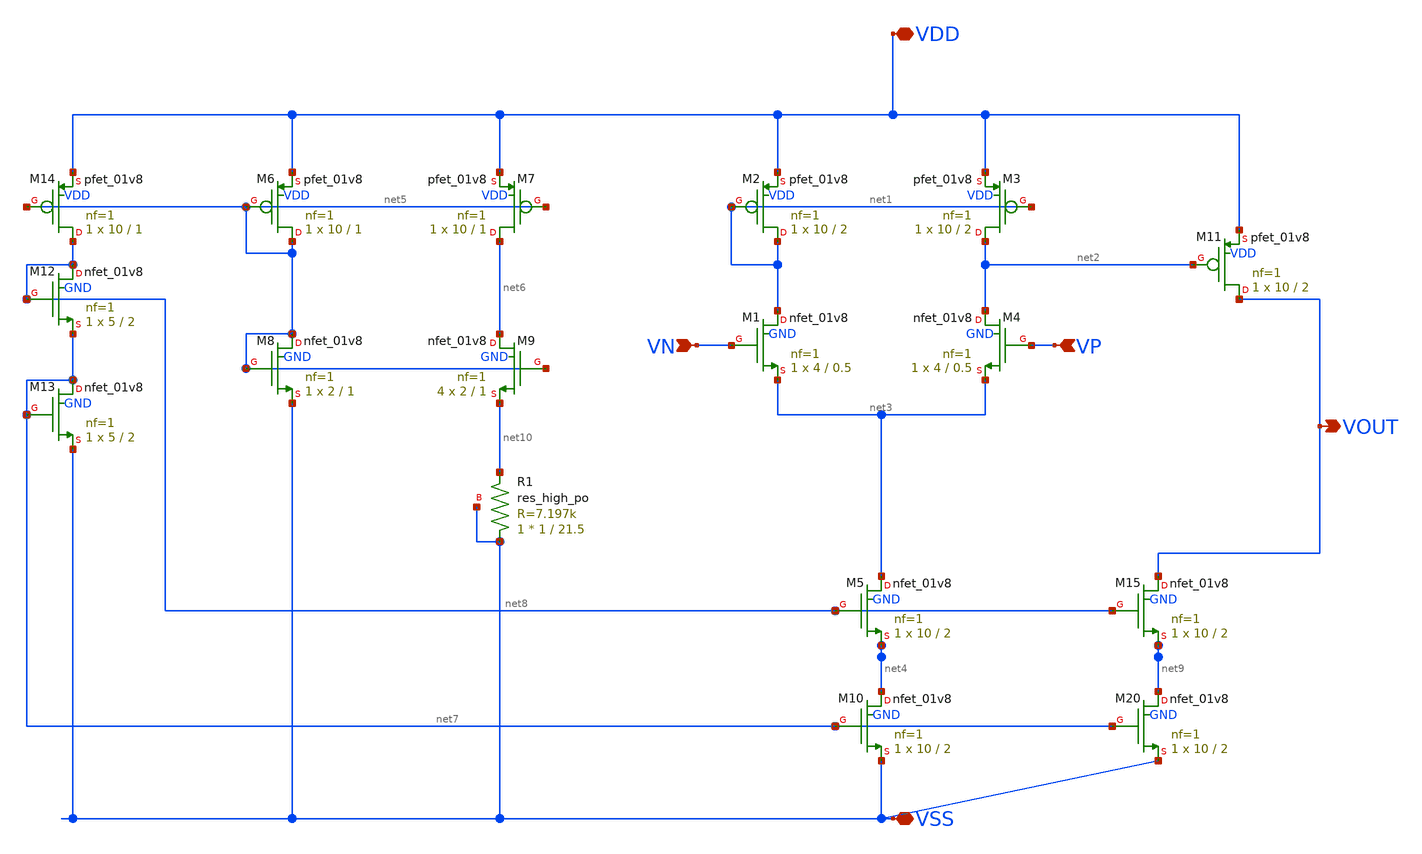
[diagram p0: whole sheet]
** sch_path: comparator.sch
**.subckt comparator VN VP VDD VOUT VSS
*.ipin VN
*.ipin VP
*.iopin VDD
*.opin VOUT
*.iopin VSS
XM2 net1 net1 VDD VDD sky130_fd_pr__pfet_01v8 L=2 W=10 nf=1 ad='int((1 + 1)/2) * 10 / 1 * 0.29' as='int((1 + 2)/2) * 10 / 1 * 0.29'
+ pd='2*int((1 + 1)/2) * (10 / 1 + 0.29)' ps='2*int((1 + 2)/2) * (10 / 1 + 0.29)' nrd='0.29 / 10 ' nrs='0.29 / 10 '
+ sa=0 sb=0 sd=0 mult=1 m=1
XM3 net2 net1 VDD VDD sky130_fd_pr__pfet_01v8 L=2 W=10 nf=1 ad='int((1 + 1)/2) * 10 / 1 * 0.29' as='int((1 + 2)/2) * 10 / 1 * 0.29'
+ pd='2*int((1 + 1)/2) * (10 / 1 + 0.29)' ps='2*int((1 + 2)/2) * (10 / 1 + 0.29)' nrd='0.29 / 10 ' nrs='0.29 / 10 '
+ sa=0 sb=0 sd=0 mult=1 m=1
XM1 net1 VN net3 GND sky130_fd_pr__nfet_01v8 L=0.5 W=4 nf=1 ad='int((1 + 1)/2) * 4 / 1 * 0.29' as='int((1 + 2)/2) * 4 / 1 * 0.29'
+ pd='2*int((1 + 1)/2) * (4 / 1 + 0.29)' ps='2*int((1 + 2)/2) * (4 / 1 + 0.29)' nrd='0.29 / 4 ' nrs='0.29 / 4 '
+ sa=0 sb=0 sd=0 mult=1 m=1
XM4 net2 VP net3 GND sky130_fd_pr__nfet_01v8 L=0.5 W=4 nf=1 ad='int((1 + 1)/2) * 4 / 1 * 0.29' as='int((1 + 2)/2) * 4 / 1 * 0.29'
+ pd='2*int((1 + 1)/2) * (4 / 1 + 0.29)' ps='2*int((1 + 2)/2) * (4 / 1 + 0.29)' nrd='0.29 / 4 ' nrs='0.29 / 4 '
+ sa=0 sb=0 sd=0 mult=1 m=1
XM5 net3 net8 net4 GND sky130_fd_pr__nfet_01v8 L=2 W=10 nf=1 ad='int((1 + 1)/2) * 10 / 1 * 0.29' as='int((1 + 2)/2) * 10 / 1 * 0.29'
+ pd='2*int((1 + 1)/2) * (10 / 1 + 0.29)' ps='2*int((1 + 2)/2) * (10 / 1 + 0.29)' nrd='0.29 / 10 ' nrs='0.29 / 10 '
+ sa=0 sb=0 sd=0 mult=1 m=1
XM6 net5 net5 VDD VDD sky130_fd_pr__pfet_01v8 L=1 W=10 nf=1 ad='int((1 + 1)/2) * 10 / 1 * 0.29' as='int((1 + 2)/2) * 10 / 1 * 0.29'
+ pd='2*int((1 + 1)/2) * (10 / 1 + 0.29)' ps='2*int((1 + 2)/2) * (10 / 1 + 0.29)' nrd='0.29 / 10 ' nrs='0.29 / 10 '
+ sa=0 sb=0 sd=0 mult=1 m=1
XM7 net6 net5 VDD VDD sky130_fd_pr__pfet_01v8 L=1 W=10 nf=1 ad='int((1 + 1)/2) * 10 / 1 * 0.29' as='int((1 + 2)/2) * 10 / 1 * 0.29'
+ pd='2*int((1 + 1)/2) * (10 / 1 + 0.29)' ps='2*int((1 + 2)/2) * (10 / 1 + 0.29)' nrd='0.29 / 10 ' nrs='0.29 / 10 '
+ sa=0 sb=0 sd=0 mult=1 m=1
XM8 net5 net5 VSS GND sky130_fd_pr__nfet_01v8 L=1 W=2 nf=1 ad='int((1 + 1)/2) * 2 / 1 * 0.29' as='int((1 + 2)/2) * 2 / 1 * 0.29'
+ pd='2*int((1 + 1)/2) * (2 / 1 + 0.29)' ps='2*int((1 + 2)/2) * (2 / 1 + 0.29)' nrd='0.29 / 2 ' nrs='0.29 / 2 '
+ sa=0 sb=0 sd=0 mult=1 m=1
XM9 net6 net5 net10 GND sky130_fd_pr__nfet_01v8 L=1 W=2 nf=1 ad='int((1 + 1)/2) * 2 / 1 * 0.29' as='int((1 + 2)/2) * 2 / 1 * 0.29'
+ pd='2*int((1 + 1)/2) * (2 / 1 + 0.29)' ps='2*int((1 + 2)/2) * (2 / 1 + 0.29)' nrd='0.29 / 2 ' nrs='0.29 / 2 '
+ sa=0 sb=0 sd=0 mult=4 m=4
XR1 VSS net10 VSS sky130_fd_pr__res_high_po W=1 L=21.5 mult=1 m=1
XM12 net8 net8 net7 GND sky130_fd_pr__nfet_01v8 L=2 W=5 nf=1 ad='int((1 + 1)/2) * 5 / 1 * 0.29' as='int((1 + 2)/2) * 5 / 1 * 0.29'
+ pd='2*int((1 + 1)/2) * (5 / 1 + 0.29)' ps='2*int((1 + 2)/2) * (5 / 1 + 0.29)' nrd='0.29 / 5 ' nrs='0.29 / 5 '
+ sa=0 sb=0 sd=0 mult=1 m=1
XM13 net7 net7 VSS GND sky130_fd_pr__nfet_01v8 L=2 W=5 nf=1 ad='int((1 + 1)/2) * 5 / 1 * 0.29' as='int((1 + 2)/2) * 5 / 1 * 0.29'
+ pd='2*int((1 + 1)/2) * (5 / 1 + 0.29)' ps='2*int((1 + 2)/2) * (5 / 1 + 0.29)' nrd='0.29 / 5 ' nrs='0.29 / 5 '
+ sa=0 sb=0 sd=0 mult=1 m=1
XM14 net8 net5 VDD VDD sky130_fd_pr__pfet_01v8 L=1 W=10 nf=1 ad='int((1 + 1)/2) * 10 / 1 * 0.29' as='int((1 + 2)/2) * 10 / 1 * 0.29'
+ pd='2*int((1 + 1)/2) * (10 / 1 + 0.29)' ps='2*int((1 + 2)/2) * (10 / 1 + 0.29)' nrd='0.29 / 10 ' nrs='0.29 / 10 '
+ sa=0 sb=0 sd=0 mult=1 m=1
XM10 net4 net7 VSS GND sky130_fd_pr__nfet_01v8 L=2 W=10 nf=1 ad='int((1 + 1)/2) * 10 / 1 * 0.29' as='int((1 + 2)/2) * 10 / 1 * 0.29'
+ pd='2*int((1 + 1)/2) * (10 / 1 + 0.29)' ps='2*int((1 + 2)/2) * (10 / 1 + 0.29)' nrd='0.29 / 10 ' nrs='0.29 / 10 '
+ sa=0 sb=0 sd=0 mult=1 m=1
XM11 VOUT net2 VDD VDD sky130_fd_pr__pfet_01v8 L=2 W=10 nf=1 ad='int((1 + 1)/2) * 10 / 1 * 0.29' as='int((1 + 2)/2) * 10 / 1 * 0.29'
+ pd='2*int((1 + 1)/2) * (10 / 1 + 0.29)' ps='2*int((1 + 2)/2) * (10 / 1 + 0.29)' nrd='0.29 / 10 ' nrs='0.29 / 10 '
+ sa=0 sb=0 sd=0 mult=1 m=1
XM15 VOUT net8 net9 GND sky130_fd_pr__nfet_01v8 L=2 W=10 nf=1 ad='int((1 + 1)/2) * 10 / 1 * 0.29' as='int((1 + 2)/2) * 10 / 1 * 0.29'
+ pd='2*int((1 + 1)/2) * (10 / 1 + 0.29)' ps='2*int((1 + 2)/2) * (10 / 1 + 0.29)' nrd='0.29 / 10 ' nrs='0.29 / 10 '
+ sa=0 sb=0 sd=0 mult=1 m=1
XM20 net9 net7 VSS GND sky130_fd_pr__nfet_01v8 L=2 W=10 nf=1 ad='int((1 + 1)/2) * 10 / 1 * 0.29' as='int((1 + 2)/2) * 10 / 1 * 0.29'
+ pd='2*int((1 + 1)/2) * (10 / 1 + 0.29)' ps='2*int((1 + 2)/2) * (10 / 1 + 0.29)' nrd='0.29 / 10 ' nrs='0.29 / 10 '
+ sa=0 sb=0 sd=0 mult=1 m=1
**.ends
.end
